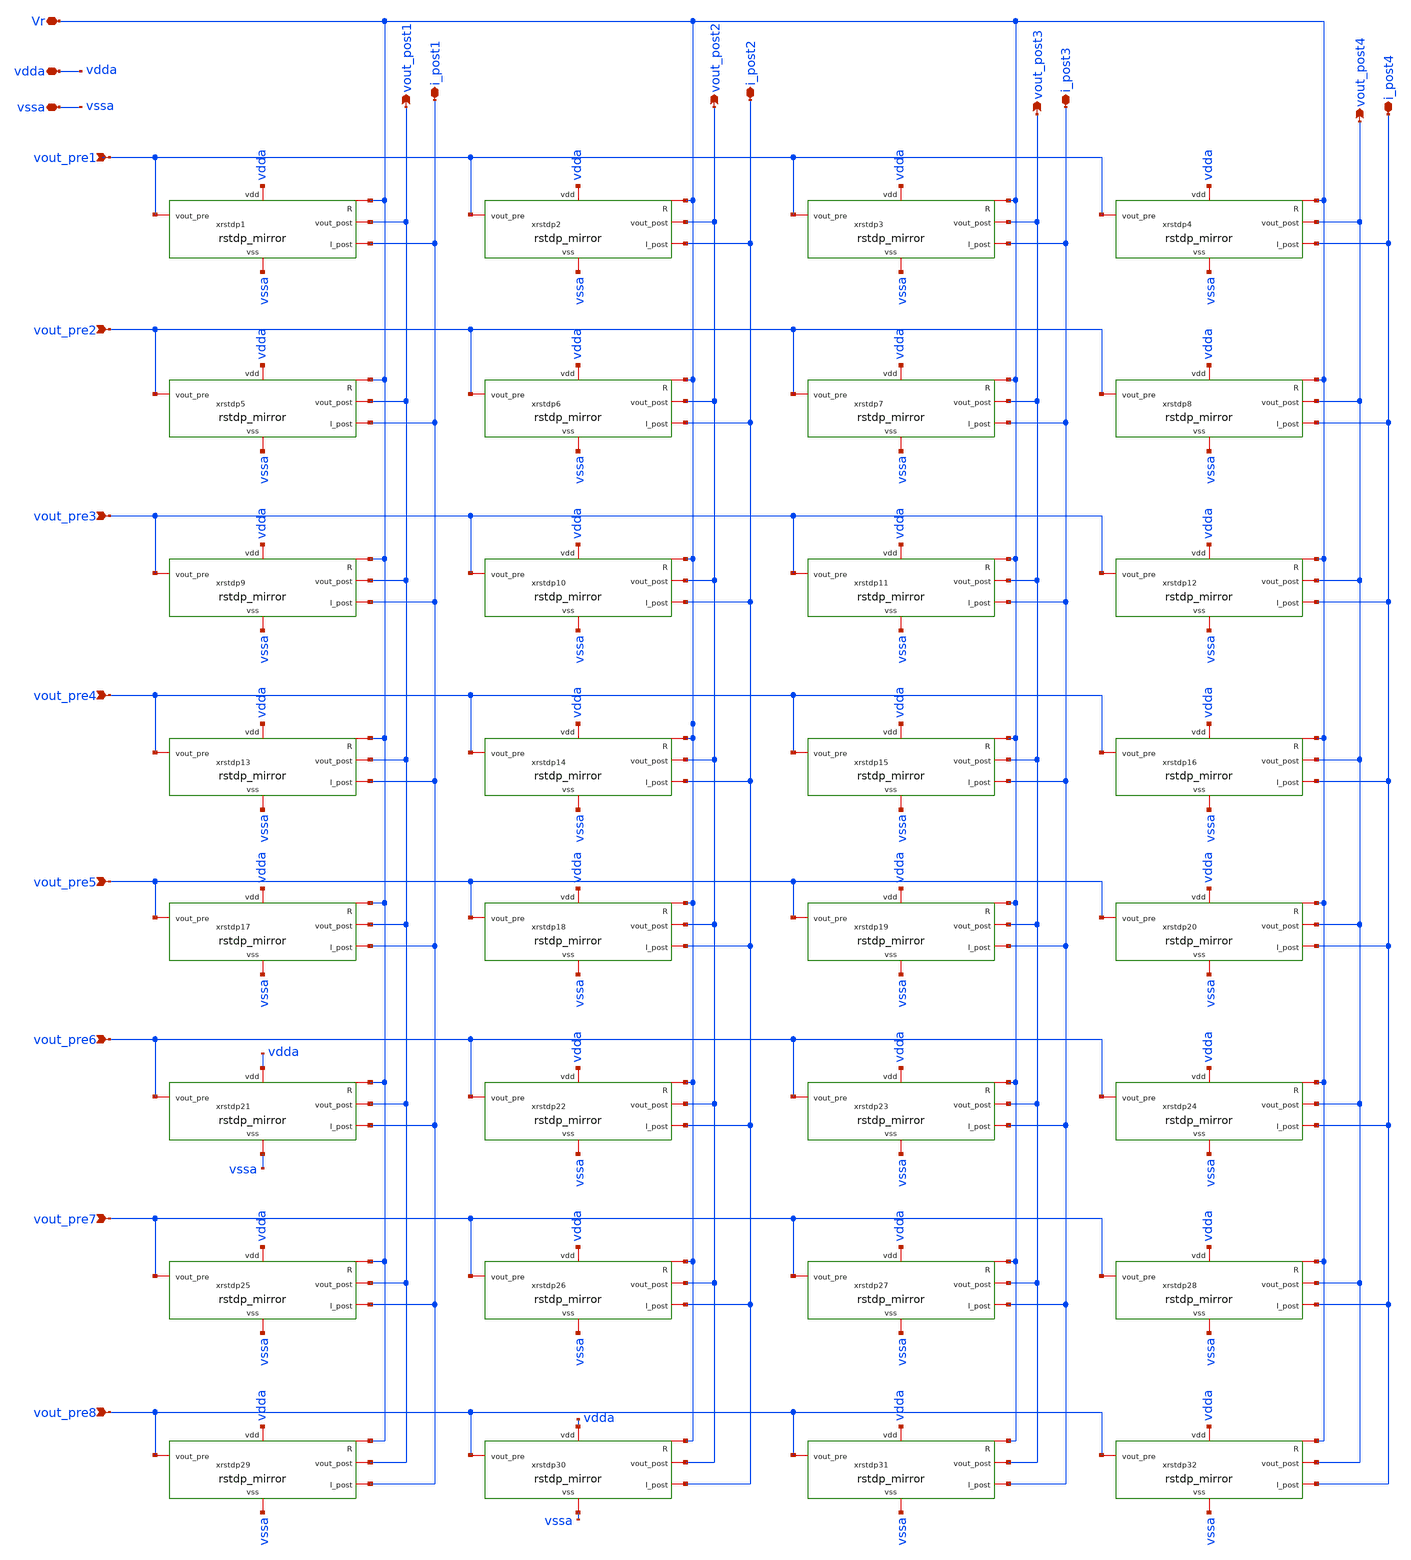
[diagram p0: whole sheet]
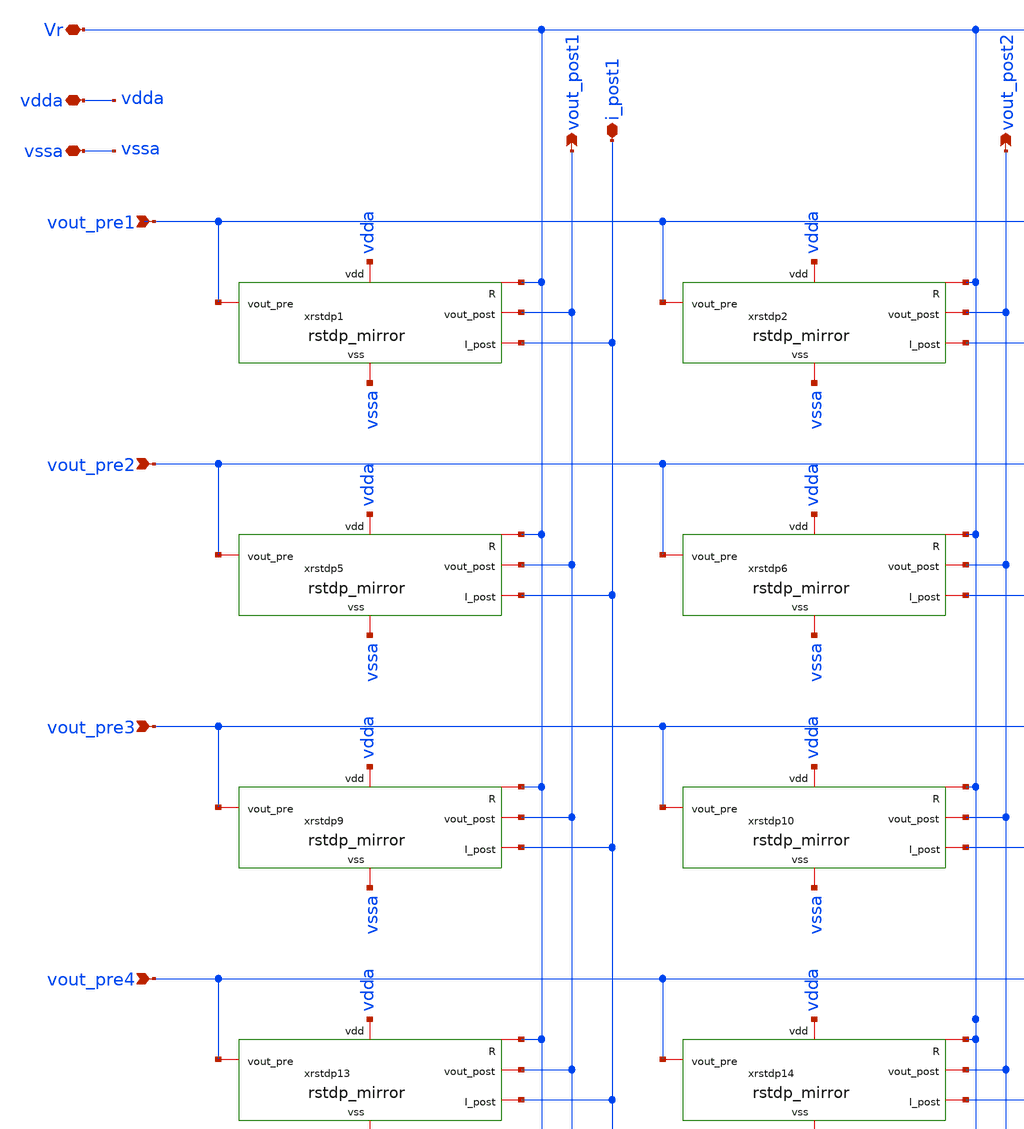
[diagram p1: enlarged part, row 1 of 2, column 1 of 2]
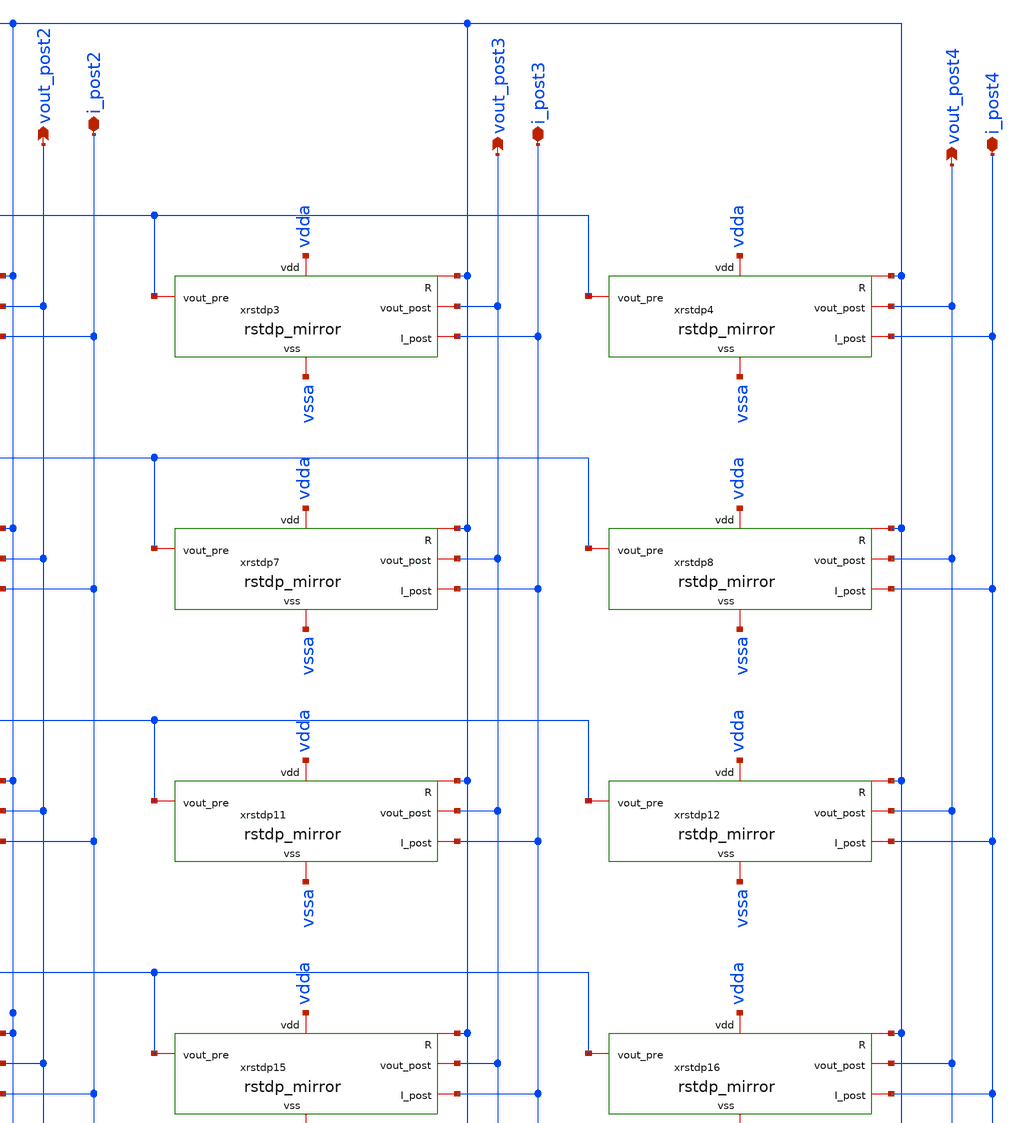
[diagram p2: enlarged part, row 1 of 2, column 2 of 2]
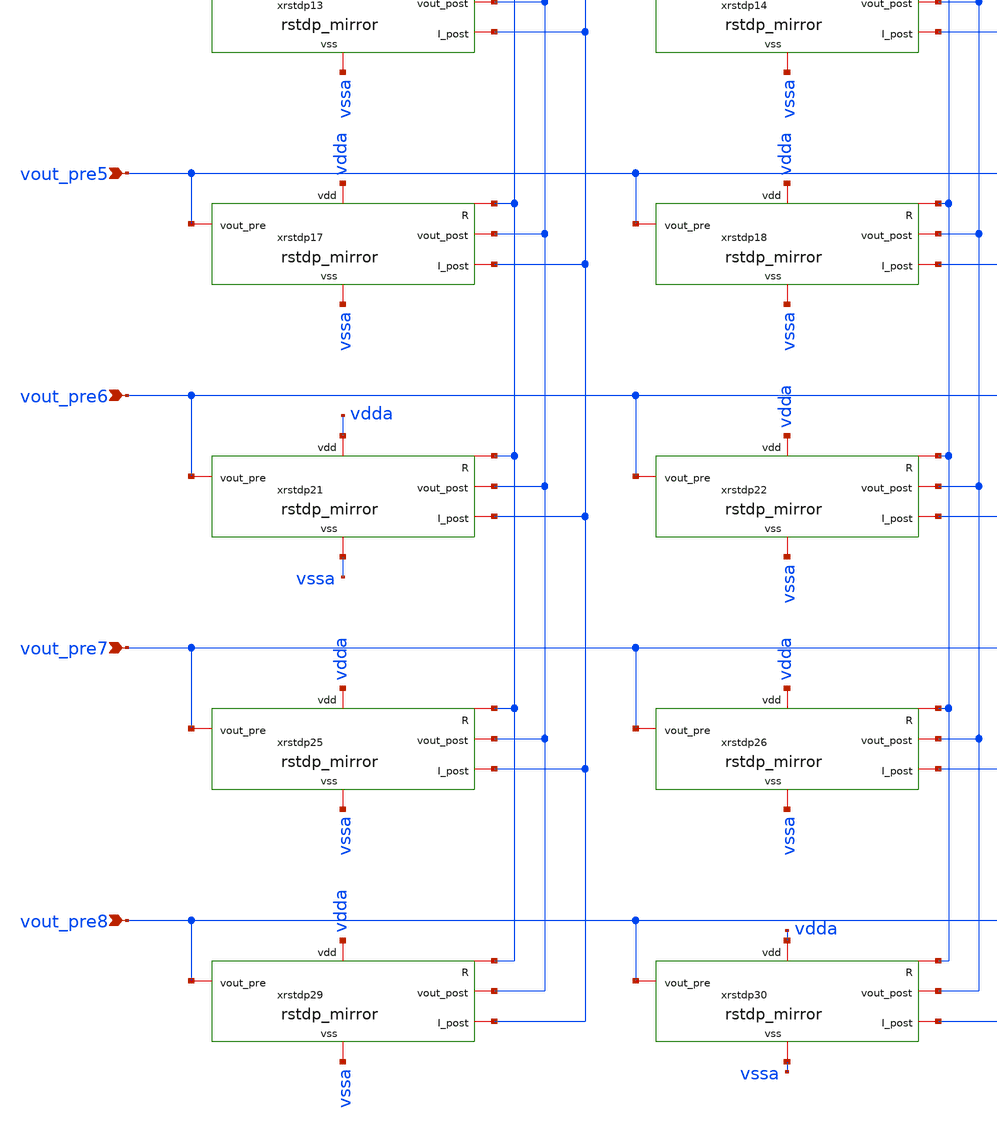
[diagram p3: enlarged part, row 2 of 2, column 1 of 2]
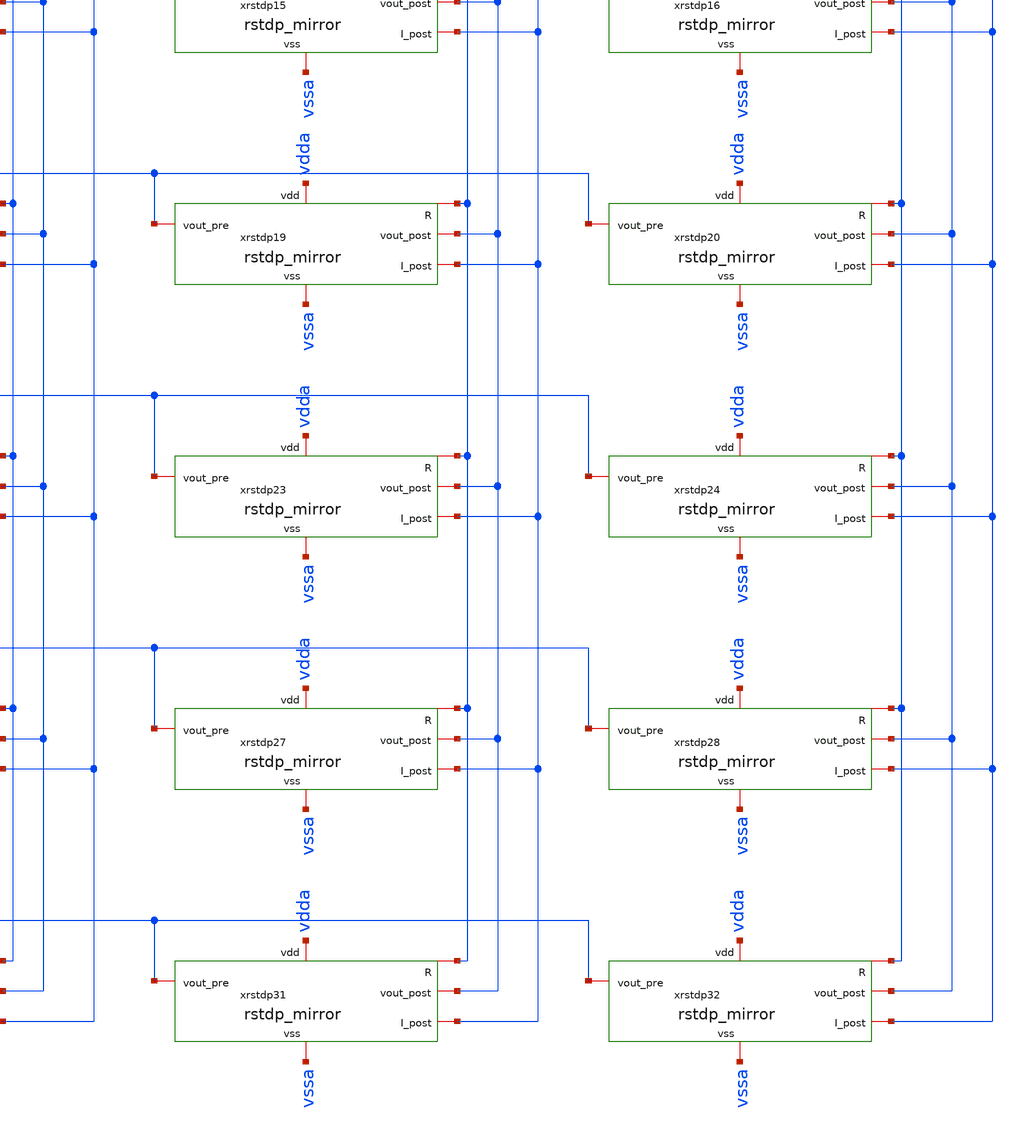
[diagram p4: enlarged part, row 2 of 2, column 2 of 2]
** sch_path: Synapse/rstdp_array_8x4.sch
**.subckt rstdp_array_8x4 vout_pre1 vout_post1 vdda vssa i_post1 i_post3 i_post4 vout_pre2 vout_pre3
*+ vout_pre4 vout_post2 vout_post3 vout_post4 i_post2 Vr vout_pre5 vout_pre6 vout_pre7 vout_pre8
*.ipin vout_pre1
*.opin vout_post1
*.iopin vdda
*.iopin vssa
*.iopin i_post1
*.iopin i_post3
*.iopin i_post4
*.ipin vout_pre2
*.ipin vout_pre3
*.ipin vout_pre4
*.opin vout_post2
*.opin vout_post3
*.opin vout_post4
*.iopin i_post2
*.iopin Vr
*.ipin vout_pre5
*.ipin vout_pre6
*.ipin vout_pre7
*.ipin vout_pre8
xrstdp1 vdda Vr vssa vout_pre1 vout_post1 i_post1 rstdp_mirror
xrstdp2 vdda Vr vssa vout_pre1 vout_post2 i_post2 rstdp_mirror
xrstdp3 vdda Vr vssa vout_pre1 vout_post3 i_post3 rstdp_mirror
xrstdp4 vdda Vr vssa vout_pre1 vout_post4 i_post4 rstdp_mirror
xrstdp5 vdda Vr vssa vout_pre2 vout_post1 i_post1 rstdp_mirror
xrstdp6 vdda Vr vssa vout_pre2 vout_post2 i_post2 rstdp_mirror
xrstdp7 vdda Vr vssa vout_pre2 vout_post3 i_post3 rstdp_mirror
xrstdp8 vdda Vr vssa vout_pre2 vout_post4 i_post4 rstdp_mirror
xrstdp9 vdda Vr vssa vout_pre3 vout_post1 i_post1 rstdp_mirror
xrstdp10 vdda Vr vssa vout_pre3 vout_post2 i_post2 rstdp_mirror
xrstdp11 vdda Vr vssa vout_pre3 vout_post3 i_post3 rstdp_mirror
xrstdp12 vdda Vr vssa vout_pre3 vout_post4 i_post4 rstdp_mirror
xrstdp13 vdda Vr vssa vout_pre4 vout_post1 i_post1 rstdp_mirror
xrstdp14 vdda Vr vssa vout_pre4 vout_post2 i_post2 rstdp_mirror
xrstdp15 vdda Vr vssa vout_pre4 vout_post3 i_post3 rstdp_mirror
xrstdp16 vdda Vr vssa vout_pre4 vout_post4 i_post4 rstdp_mirror
xrstdp17 vdda Vr vssa vout_pre5 vout_post1 i_post1 rstdp_mirror
xrstdp18 vdda Vr vssa vout_pre5 vout_post2 i_post2 rstdp_mirror
xrstdp19 vdda Vr vssa vout_pre5 vout_post3 i_post3 rstdp_mirror
xrstdp20 vdda Vr vssa vout_pre5 vout_post4 i_post4 rstdp_mirror
xrstdp21 vdda Vr vssa vout_pre6 vout_post1 i_post1 rstdp_mirror
xrstdp22 vdda Vr vssa vout_pre6 vout_post2 i_post2 rstdp_mirror
xrstdp23 vdda Vr vssa vout_pre6 vout_post3 i_post3 rstdp_mirror
xrstdp24 vdda Vr vssa vout_pre6 vout_post4 i_post4 rstdp_mirror
xrstdp25 vdda Vr vssa vout_pre7 vout_post1 i_post1 rstdp_mirror
xrstdp26 vdda Vr vssa vout_pre7 vout_post2 i_post2 rstdp_mirror
xrstdp27 vdda Vr vssa vout_pre7 vout_post3 i_post3 rstdp_mirror
xrstdp28 vdda Vr vssa vout_pre7 vout_post4 i_post4 rstdp_mirror
xrstdp29 vdda Vr vssa vout_pre8 vout_post1 i_post1 rstdp_mirror
xrstdp30 vdda Vr vssa vout_pre8 vout_post2 i_post2 rstdp_mirror
xrstdp31 vdda Vr vssa vout_pre8 vout_post3 i_post3 rstdp_mirror
xrstdp32 vdda Vr vssa vout_pre8 vout_post4 i_post4 rstdp_mirror
**.ends

* expanding   symbol:  Synapse/rstdp_mirror.sym # of pins=6
** sym_path: Synapse/rstdp_mirror.sym
** sch_path: Synapse/rstdp_mirror.sch
.subckt rstdp_mirror vdd R vss vout_pre vout_post I_post
*.iopin vdd
*.iopin vss
*.iopin R
*.iopin vout_post
*.iopin vout_pre
*.iopin I_post
XM2 A vout_pre vpre vss sky130_fd_pr__nfet_01v8 L=0.15 W=7.5 nf=1 ad='int((nf+1)/2) * W/nf * 0.29' as='int((nf+2)/2) * W/nf * 0.29'
+ pd='2*int((nf+1)/2) * (W/nf + 0.29)' ps='2*int((nf+2)/2) * (W/nf + 0.29)' nrd='0.29 / W' nrs='0.29 / W'
+ sa=0 sb=0 sd=0 mult=1 m=1
XM3 vpre vout_post vss vss sky130_fd_pr__nfet_01v8 L=0.15 W=7.5 nf=1 ad='int((nf+1)/2) * W/nf * 0.29'
+ as='int((nf+2)/2) * W/nf * 0.29' pd='2*int((nf+1)/2) * (W/nf + 0.29)' ps='2*int((nf+2)/2) * (W/nf + 0.29)'
+ nrd='0.29 / W' nrs='0.29 / W' sa=0 sb=0 sd=0 mult=1 m=1
XM1 A vout_post vpost vss sky130_fd_pr__nfet_01v8 L=0.15 W=7.5 nf=1 ad='int((nf+1)/2) * W/nf * 0.29'
+ as='int((nf+2)/2) * W/nf * 0.29' pd='2*int((nf+1)/2) * (W/nf + 0.29)' ps='2*int((nf+2)/2) * (W/nf + 0.29)'
+ nrd='0.29 / W' nrs='0.29 / W' sa=0 sb=0 sd=0 mult=1 m=1
XM4 vpost vout_pre vss vss sky130_fd_pr__nfet_01v8 L=0.15 W=7.5 nf=1 ad='int((nf+1)/2) * W/nf * 0.29'
+ as='int((nf+2)/2) * W/nf * 0.29' pd='2*int((nf+1)/2) * (W/nf + 0.29)' ps='2*int((nf+2)/2) * (W/nf + 0.29)'
+ nrd='0.29 / W' nrs='0.29 / W' sa=0 sb=0 sd=0 mult=1 m=1
XR2 te be rram_v0
XM5 vpre R te vss sky130_fd_pr__nfet_01v8 L=0.15 W=7.5 nf=1 ad='int((nf+1)/2) * W/nf * 0.29' as='int((nf+2)/2) * W/nf * 0.29'
+ pd='2*int((nf+1)/2) * (W/nf + 0.29)' ps='2*int((nf+2)/2) * (W/nf + 0.29)' nrd='0.29 / W' nrs='0.29 / W'
+ sa=0 sb=0 sd=0 mult=1 m=1
XM6 net1 R vpost vss sky130_fd_pr__nfet_01v8 L=0.15 W=7.5 nf=1 ad='int((nf+1)/2) * W/nf * 0.29' as='int((nf+2)/2) * W/nf * 0.29'
+ pd='2*int((nf+1)/2) * (W/nf + 0.29)' ps='2*int((nf+2)/2) * (W/nf + 0.29)' nrd='0.29 / W' nrs='0.29 / W'
+ sa=0 sb=0 sd=0 mult=1 m=1
XM7 vpre R net1 vdd sky130_fd_pr__pfet_01v8 L=0.15 W=15 nf=1 ad='int((nf+1)/2) * W/nf * 0.29' as='int((nf+2)/2) * W/nf * 0.29'
+ pd='2*int((nf+1)/2) * (W/nf + 0.29)' ps='2*int((nf+2)/2) * (W/nf + 0.29)' nrd='0.29 / W' nrs='0.29 / W'
+ sa=0 sb=0 sd=0 mult=1 m=1
XM8 te R vpost vdd sky130_fd_pr__pfet_01v8 L=0.15 W=15 nf=1 ad='int((nf+1)/2) * W/nf * 0.29' as='int((nf+2)/2) * W/nf * 0.29'
+ pd='2*int((nf+1)/2) * (W/nf + 0.29)' ps='2*int((nf+2)/2) * (W/nf + 0.29)' nrd='0.29 / W' nrs='0.29 / W'
+ sa=0 sb=0 sd=0 mult=1 m=1
XM14 net2 A vdd vdd sky130_fd_pr__pfet_01v8 L=30 W=0.5 nf=1 ad='int((nf+1)/2) * W/nf * 0.29' as='int((nf+2)/2) * W/nf * 0.29'
+ pd='2*int((nf+1)/2) * (W/nf + 0.29)' ps='2*int((nf+2)/2) * (W/nf + 0.29)' nrd='0.29 / W' nrs='0.29 / W'
+ sa=0 sb=0 sd=0 mult=1 m=1
XM15 A A vdd vdd sky130_fd_pr__pfet_01v8 L=0.15 W=2.5 nf=1 ad='int((nf+1)/2) * W/nf * 0.29' as='int((nf+2)/2) * W/nf * 0.29'
+ pd='2*int((nf+1)/2) * (W/nf + 0.29)' ps='2*int((nf+2)/2) * (W/nf + 0.29)' nrd='0.29 / W' nrs='0.29 / W'
+ sa=0 sb=0 sd=0 mult=1 m=1
**** begin user architecture code


.save v(te) v(be) i(vmr)


**** end user architecture code
Vmr be net1 0
.save i(vmr)
XM9 I_post A net2 vdd sky130_fd_pr__pfet_01v8 L=30 W=0.5 nf=1 ad='int((nf+1)/2) * W/nf * 0.29' as='int((nf+2)/2) * W/nf * 0.29'
+ pd='2*int((nf+1)/2) * (W/nf + 0.29)' ps='2*int((nf+2)/2) * (W/nf + 0.29)' nrd='0.29 / W' nrs='0.29 / W'
+ sa=0 sb=0 sd=0 mult=1 m=1
.ends

.end
